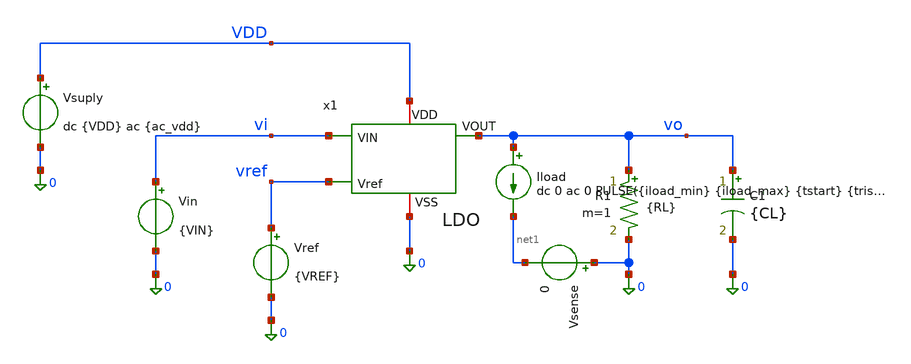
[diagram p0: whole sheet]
** sch_path: xschem/ldo_tb.sch
**.subckt ldo_tb
x1 vi vo VDD vref 0 LDO
Vsuply VDD 0 dc {VDD} ac {ac_vdd}
Vref vref 0 {VREF}
Vin vi 0 {VIN}
R1 vo 0 {RL} m=1
C1 vo 0 {CL} m=1
Iload vo net1 dc 0 ac 0 PULSE({iload_min} {iload_max} {tstart} {trise} {tfall} {twidth} {tperiod})
Vsense 0 net1 0
**** begin user architecture code




* 1. Inclusión de libreria de modelos Sky130 PRIMERO
.lib /foss/pdks/sky130A/libs.tech/ngspice/sky130.lib.spice tt
.option temp=125
.option num_threads=8

**parametros_ldo
.param VDD = 1.8
.param VREF = 0.6
.param VIN = 1.8
.param RL = 25
.param CL = 1u
.param tsim = 2m
* Parámetros para la prueba de carga del LDO
.param iload_min = 1m
.param iload_max = 50m
.param tstart   = 10u
.param trise    = 100n
.param tfall    = 100n
.param twidth   = 200u
.param tperiod  = 400u
.param tperiod  = 400u
.param tsim = '5*tperiod'

.param ac_iprobe = 1
.param ac_vdd = 0




.control
let tperiod  = 400u
let tsim = '5*tperiod'

set filetype=ascii

* 1. Punto de Operación (.OP)
op
write LDO_op.raw

* 2. Análisis Transitorio para overshot y undershot (.TRAN)
tran 1u $&tsim
write LDO_tran_picos.raw

* 3. Análisis en Frecuencia  para estabilidad (.AC)
ac dec 10 1 1G
* 1. Ganancia de Lazo Abierto T(s) = v(x1.vre) / v(x1.net3)
let T_loop = v(x1.vre) / v(x1.net3)
let loop_gain_db = vdb(T_loop)
let fase_deg = vp(T_loop) * 180 / pi
write LDO_ac_estability.raw

* 4. Análisis en dc sweep para el load regulation
dc iload 100u 50m 100u
*plot vo
*plot vsense#branch
write LDO_dc_load.raw

* 5. Analisis en dc sweep para el line regulation
dc vin 1.3 2 0.01
*plot vo
*plot vi
write LDO_dc_line.raw

*6. análisis en Frecuencia (.AC) para el PSRR
alterparam ac_iprobe = 0
alterparam ac_vdd = 1
reset

ac dec 10 1 1G
* 1. Ganancia de Lazo Abierto T(s) = v(x1.vre) / v(x1.net3)
let psrr1 = v(vdd)/v(vo)
let psrr_db = vdb(psrr1)

write LDO_ac_psrr.raw





*CALCULOS PARA ESTABILIDAD Y GANANCIA EN LAZO ABIERTO

setplot ac1
* 2. UGB (Frecuencia donde la magnitud cruza 0 dB)
meas ac ugb WHEN loop_gain_db = 0.0
* 3. Medir la fase en grados en el punto exacto del UGB
meas ac fase_ugb FIND fase_deg WHEN loop_gain_db = 0.0

* 4. Calcular el Margen de Fase (PM = fase_ugb)
let margen_fase = fase_ugb
meas ac ganancia_banda_plana   find loop_gain_db at=1
echo 'margen_fase = $&fase_ugb'

*CALCULOS PARA EL PSRR
setplot ac2
meas ac gananciaPSRR_1   find psrr_db at=1
meas ac gananciaPSRR_1k  find psrr_db at=1k
meas ac gananciaPSRR_10k find psrr_db at=10k
meas ac gananciaPSRR_1M  find psrr_db at=1Meg

*CALCULOS PARA EL LOAD REGULATION
setplot dc1
meas dc voload_max MAX v(vo)
meas dc voload_min MIN v(vo)
let load_regulation = voload_max - voload_min
echo 'load_regulation = $&load_regulation'

*CALCULOS PARA EL LINE REGULATION
setplot dc2
meas dc voline_max MAX v(vo)
meas dc voline_min MIN v(vo)
let line_regulation = voline_max - voline_min
echo 'line_regulation = $&line_regulation'


.endc



**** end user architecture code
**.ends

* expanding   symbol:  /foss/designs/LDO-sky130/xschem/LDO.sym # of pins=5
** sym_path: xschem/LDO.sym
** sch_path: xschem/LDO.sch
.subckt LDO VIN VOUT VDD Vref VSS
*.ipin VIN
*.iopin VDD
*.opin VOUT
*.ipin Vref
*.iopin VSS
x1 VDD net2 Vref net3 net1 VSS OTA
I0 VDD net1 10u
XM1 VOUT net2 VIN VDD sky130_fd_pr__pfet_01v8_lvt L=0.35 W=1000 nf=50 ad='int((50 + 1)/2) * 1000 / 50 * 0.29'
+ as='int((50 + 2)/2) * 1000 / 50 * 0.29' pd='2*int((50 + 1)/2) * (1000 / 50 + 0.29)' ps='2*int((50 + 2)/2) * (1000 / 50 + 0.29)'
+ nrd='0.29 / 1000 ' nrs='0.29 / 1000 ' sa=0 sb=0 sd=0 mult=5 m=5
XR1 Vre VOUT VDD sky130_fd_pr__res_iso_pw W=0.35 L=10 m=1
XR2 VSS Vre VDD sky130_fd_pr__res_iso_pw W=0.35 L=10 m=1
V1 net3 Vre 0 ac {ac_iprobe}
XC1 VOUT Vre sky130_fd_pr__cap_mim_m3_2 W=19.5 L=19.5 MF=1 m=1
.ends


* expanding   symbol:  /foss/designs/LDO-sky130/xschem/OTA.sym # of pins=6
** sym_path: xschem/OTA.sym
** sch_path: xschem/OTA.sch
.subckt OTA VDD VO_ota VIN_ota VIP_ota Iref VSS
*.ipin VIN_ota
*.opin VO_ota
*.iopin Iref
*.iopin VSS
*.iopin VDD
*.ipin VIP_ota
XMr Iref Iref VSS VSS sky130_fd_pr__nfet_01v8 L=0.5 W=0.5 nf=1 ad='int((1 + 1)/2) * 0.5 / 1 * 0.29' as='int((1 + 2)/2) * 0.5 / 1 * 0.29'
+ pd='2*int((1 + 1)/2) * (0.5 / 1 + 0.29)' ps='2*int((1 + 2)/2) * (0.5 / 1 + 0.29)' nrd='0.29 / 0.5 ' nrs='0.29 / 0.5 '
+ sa=0 sb=0 sd=0 mult=1 m=1
XMo VO_ota VO_ota1 VDD VDD sky130_fd_pr__pfet_01v8 L=0.5 W=20 nf=1 ad='int((1 + 1)/2) * 20 / 1 * 0.29'
+ as='int((1 + 2)/2) * 20 / 1 * 0.29' pd='2*int((1 + 1)/2) * (20 / 1 + 0.29)' ps='2*int((1 + 2)/2) * (20 / 1 + 0.29)'
+ nrd='0.29 / 20 ' nrs='0.29 / 20 ' sa=0 sb=0 sd=0 mult=1 m=1
XMrc1 Vtail Iref VSS VSS sky130_fd_pr__nfet_01v8 L=0.5 W=2 nf=1 ad='int((1 + 1)/2) * 2 / 1 * 0.29' as='int((1 + 2)/2) * 2 / 1 * 0.29'
+ pd='2*int((1 + 1)/2) * (2 / 1 + 0.29)' ps='2*int((1 + 2)/2) * (2 / 1 + 0.29)' nrd='0.29 / 2 ' nrs='0.29 / 2 '
+ sa=0 sb=0 sd=0 mult=1 m=1
XMc2 VO_ota Iref VSS VSS sky130_fd_pr__nfet_01v8 L=0.5 W=1 nf=1 ad='int((1 + 1)/2) * 1 / 1 * 0.29' as='int((1 + 2)/2) * 1 / 1 * 0.29'
+ pd='2*int((1 + 1)/2) * (1 / 1 + 0.29)' ps='2*int((1 + 2)/2) * (1 / 1 + 0.29)' nrd='0.29 / 1 ' nrs='0.29 / 1 '
+ sa=0 sb=0 sd=0 mult=1 m=1
XMn VGP VIN_ota Vtail VSS sky130_fd_pr__nfet_01v8 L=0.5 W=40 nf=1 ad='int((1 + 1)/2) * 40 / 1 * 0.29'
+ as='int((1 + 2)/2) * 40 / 1 * 0.29' pd='2*int((1 + 1)/2) * (40 / 1 + 0.29)' ps='2*int((1 + 2)/2) * (40 / 1 + 0.29)'
+ nrd='0.29 / 40 ' nrs='0.29 / 40 ' sa=0 sb=0 sd=0 mult=1 m=1
XMp VO_ota1 VIP_ota Vtail VSS sky130_fd_pr__nfet_01v8 L=0.5 W=40 nf=1 ad='int((1 + 1)/2) * 40 / 1 * 0.29'
+ as='int((1 + 2)/2) * 40 / 1 * 0.29' pd='2*int((1 + 1)/2) * (40 / 1 + 0.29)' ps='2*int((1 + 2)/2) * (40 / 1 + 0.29)'
+ nrd='0.29 / 40 ' nrs='0.29 / 40 ' sa=0 sb=0 sd=0 mult=1 m=1
XMpr VO_ota1 VGP VDD VDD sky130_fd_pr__pfet_01v8 L=0.5 W=40 nf=1 ad='int((1 + 1)/2) * 40 / 1 * 0.29'
+ as='int((1 + 2)/2) * 40 / 1 * 0.29' pd='2*int((1 + 1)/2) * (40 / 1 + 0.29)' ps='2*int((1 + 2)/2) * (40 / 1 + 0.29)'
+ nrd='0.29 / 40 ' nrs='0.29 / 40 ' sa=0 sb=0 sd=0 mult=1 m=1
XMnr VGP VGP VDD VDD sky130_fd_pr__pfet_01v8 L=0.5 W=40 nf=1 ad='int((1 + 1)/2) * 40 / 1 * 0.29' as='int((1 + 2)/2) * 40 / 1 * 0.29'
+ pd='2*int((1 + 1)/2) * (40 / 1 + 0.29)' ps='2*int((1 + 2)/2) * (40 / 1 + 0.29)' nrd='0.29 / 40 ' nrs='0.29 / 40 '
+ sa=0 sb=0 sd=0 mult=1 m=1
XR1 VO_ota1 net1 VDD sky130_fd_pr__res_high_po W=0.35 L=360 mult=1 m=1
XC1 VO_ota net1 sky130_fd_pr__cap_mim_m3_2 W=50 L=50 MF=1 m=1
.ends

.end
